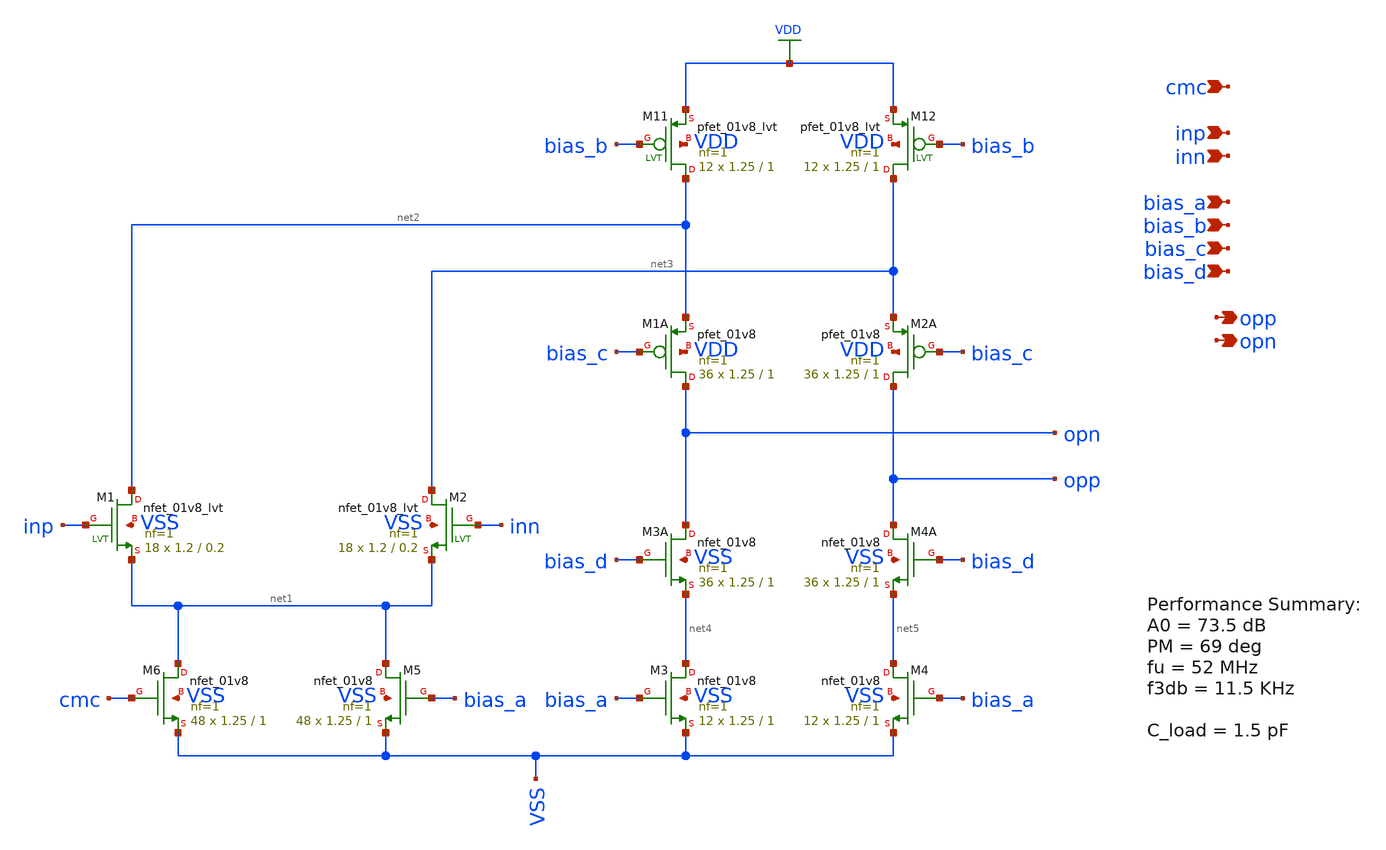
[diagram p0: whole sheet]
** sch_path: design/schematic/folded_cascode_core_73dB_69degPM.sch
**.subckt folded_cascode_core_73dB_69degPM cmc inp inn bias_a bias_b bias_c bias_d opp opn
*.ipin cmc
*.ipin inp
*.ipin inn
*.ipin bias_a
*.ipin bias_b
*.ipin bias_c
*.ipin bias_d
*.opin opp
*.opin opn
XM1 net2 inp net1 VSS sky130_fd_pr__nfet_01v8_lvt L=0.2 W=1.2 nf=1 ad='int((nf+1)/2) * W/nf * 0.29' as='int((nf+2)/2) * W/nf * 0.29'
+ pd='2*int((nf+1)/2) * (W/nf + 0.29)' ps='2*int((nf+2)/2) * (W/nf + 0.29)' nrd='0.29 / W' nrs='0.29 / W'
+ sa=0 sb=0 sd=0 mult=18 m=18
XM2 net3 inn net1 VSS sky130_fd_pr__nfet_01v8_lvt L=0.2 W=1.2 nf=1 ad='int((nf+1)/2) * W/nf * 0.29' as='int((nf+2)/2) * W/nf * 0.29'
+ pd='2*int((nf+1)/2) * (W/nf + 0.29)' ps='2*int((nf+2)/2) * (W/nf + 0.29)' nrd='0.29 / W' nrs='0.29 / W'
+ sa=0 sb=0 sd=0 mult=18 m=18
XM6 net1 cmc VSS VSS sky130_fd_pr__nfet_01v8 L=1 W=1.25 nf=1 ad='int((nf+1)/2) * W/nf * 0.29' as='int((nf+2)/2) * W/nf * 0.29'
+ pd='2*int((nf+1)/2) * (W/nf + 0.29)' ps='2*int((nf+2)/2) * (W/nf + 0.29)' nrd='0.29 / W' nrs='0.29 / W'
+ sa=0 sb=0 sd=0 mult=48 m=48
XM5 net1 bias_a VSS VSS sky130_fd_pr__nfet_01v8 L=1 W=1.25 nf=1 ad='int((nf+1)/2) * W/nf * 0.29' as='int((nf+2)/2) * W/nf * 0.29'
+ pd='2*int((nf+1)/2) * (W/nf + 0.29)' ps='2*int((nf+2)/2) * (W/nf + 0.29)' nrd='0.29 / W' nrs='0.29 / W'
+ sa=0 sb=0 sd=0 mult=48 m=48
XM11 net2 bias_b VDD VDD sky130_fd_pr__pfet_01v8_lvt L=1 W=1.25 nf=1 ad='int((nf+1)/2) * W/nf * 0.29'
+ as='int((nf+2)/2) * W/nf * 0.29' pd='2*int((nf+1)/2) * (W/nf + 0.29)' ps='2*int((nf+2)/2) * (W/nf + 0.29)'
+ nrd='0.29 / W' nrs='0.29 / W' sa=0 sb=0 sd=0 mult=12 m=12
XM12 net3 bias_b VDD VDD sky130_fd_pr__pfet_01v8_lvt L=1 W=1.25 nf=1 ad='int((nf+1)/2) * W/nf * 0.29'
+ as='int((nf+2)/2) * W/nf * 0.29' pd='2*int((nf+1)/2) * (W/nf + 0.29)' ps='2*int((nf+2)/2) * (W/nf + 0.29)'
+ nrd='0.29 / W' nrs='0.29 / W' sa=0 sb=0 sd=0 mult=12 m=12
XM1A opn bias_c net2 VDD sky130_fd_pr__pfet_01v8 L=1 W=1.25 nf=1 ad='int((nf+1)/2) * W/nf * 0.29' as='int((nf+2)/2) * W/nf * 0.29'
+ pd='2*int((nf+1)/2) * (W/nf + 0.29)' ps='2*int((nf+2)/2) * (W/nf + 0.29)' nrd='0.29 / W' nrs='0.29 / W'
+ sa=0 sb=0 sd=0 mult=36 m=36
XM2A opp bias_c net3 VDD sky130_fd_pr__pfet_01v8 L=1 W=1.25 nf=1 ad='int((nf+1)/2) * W/nf * 0.29' as='int((nf+2)/2) * W/nf * 0.29'
+ pd='2*int((nf+1)/2) * (W/nf + 0.29)' ps='2*int((nf+2)/2) * (W/nf + 0.29)' nrd='0.29 / W' nrs='0.29 / W'
+ sa=0 sb=0 sd=0 mult=36 m=36
XM3A opn bias_d net4 VSS sky130_fd_pr__nfet_01v8 L=1 W=1.25 nf=1 ad='int((nf+1)/2) * W/nf * 0.29' as='int((nf+2)/2) * W/nf * 0.29'
+ pd='2*int((nf+1)/2) * (W/nf + 0.29)' ps='2*int((nf+2)/2) * (W/nf + 0.29)' nrd='0.29 / W' nrs='0.29 / W'
+ sa=0 sb=0 sd=0 mult=36 m=36
XM4A opp bias_d net5 VSS sky130_fd_pr__nfet_01v8 L=1 W=1.25 nf=1 ad='int((nf+1)/2) * W/nf * 0.29' as='int((nf+2)/2) * W/nf * 0.29'
+ pd='2*int((nf+1)/2) * (W/nf + 0.29)' ps='2*int((nf+2)/2) * (W/nf + 0.29)' nrd='0.29 / W' nrs='0.29 / W'
+ sa=0 sb=0 sd=0 mult=36 m=36
XM3 net4 bias_a VSS VSS sky130_fd_pr__nfet_01v8 L=1 W=1.25 nf=1 ad='int((nf+1)/2) * W/nf * 0.29' as='int((nf+2)/2) * W/nf * 0.29'
+ pd='2*int((nf+1)/2) * (W/nf + 0.29)' ps='2*int((nf+2)/2) * (W/nf + 0.29)' nrd='0.29 / W' nrs='0.29 / W'
+ sa=0 sb=0 sd=0 mult=12 m=12
XM4 net5 bias_a VSS VSS sky130_fd_pr__nfet_01v8 L=1 W=1.25 nf=1 ad='int((nf+1)/2) * W/nf * 0.29' as='int((nf+2)/2) * W/nf * 0.29'
+ pd='2*int((nf+1)/2) * (W/nf + 0.29)' ps='2*int((nf+2)/2) * (W/nf + 0.29)' nrd='0.29 / W' nrs='0.29 / W'
+ sa=0 sb=0 sd=0 mult=12 m=12
**.ends
.GLOBAL VDD
.end
